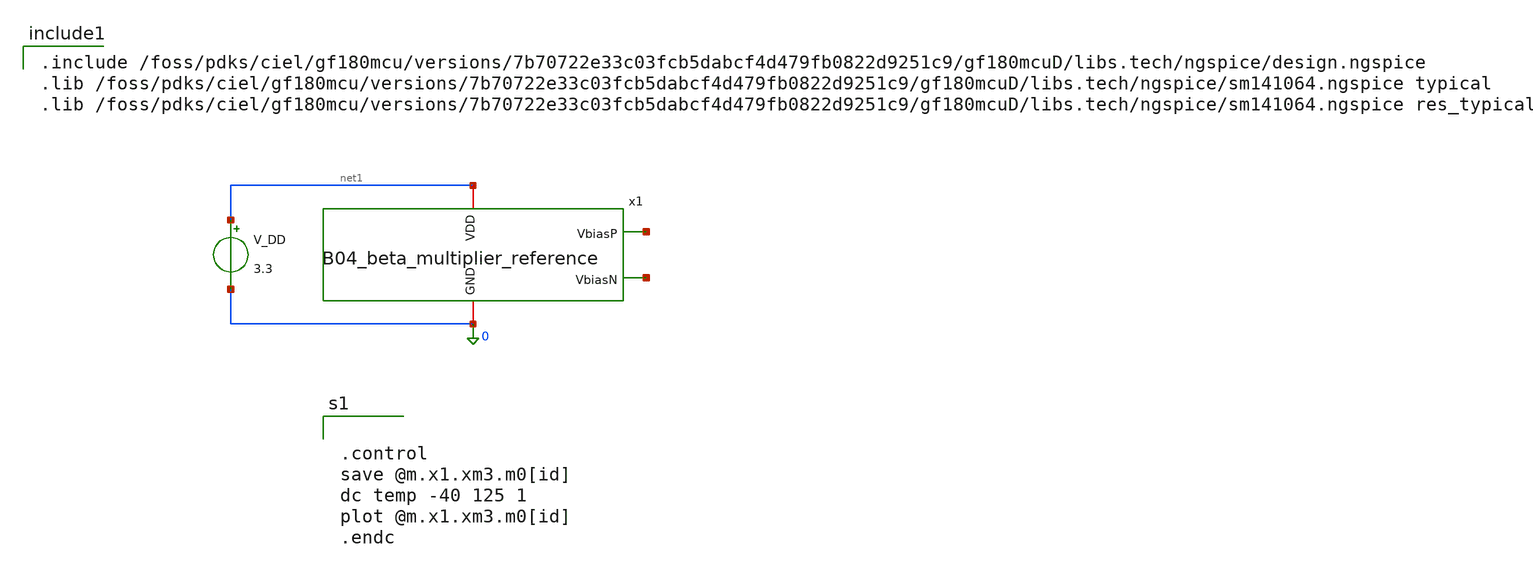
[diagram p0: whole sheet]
** sch_path: analog/B04_tb_beta_multiplier_reference.sch
**.subckt B04_tb_beta_multiplier_reference
x1 net1 net2 net3 0 B04_beta_multiplier_reference length=410u
V_DD net1 0 3.3
**** begin user architecture code


.control
save @m.x1.xm3.m0[id]
dc temp -40 125 1
plot @m.x1.xm3.m0[id]
.endc



.include /foss/pdks/ciel/gf180mcu/versions/7b70722e33c03fcb5dabcf4d479fb0822d9251c9/gf180mcuD/libs.tech/ngspice/design.ngspice
.lib /foss/pdks/ciel/gf180mcu/versions/7b70722e33c03fcb5dabcf4d479fb0822d9251c9/gf180mcuD/libs.tech/ngspice/sm141064.ngspice typical
.lib /foss/pdks/ciel/gf180mcu/versions/7b70722e33c03fcb5dabcf4d479fb0822d9251c9/gf180mcuD/libs.tech/ngspice/sm141064.ngspice res_typical

**** end user architecture code
**.ends

* expanding   symbol:
*+  AURA-Event-Driven-Mixed-Signal-ASIC-for-Acoustic-Pattern-Detection/analog/B04_beta_multiplier_reference.sym # of pins=4
** sym_path: analog/B04_beta_multiplier_reference.sym
** sch_path: analog/B04_beta_multiplier_reference.sch
.subckt B04_beta_multiplier_reference VDD VbiasP VbiasN GND  length=410u
*.iopin VDD
*.iopin GND
*.opin VbiasP
*.opin VbiasN
XM2 VbiasN VbiasP VDD VDD pfet_03v3 L=4u W=2u nf=1 ad='int((nf+1)/2) * W/nf * 0.18u' as='int((nf+2)/2) * W/nf * 0.18u'
+ pd='2*int((nf+1)/2) * (W/nf + 0.18u)' ps='2*int((nf+2)/2) * (W/nf + 0.18u)' nrd='0.18u / W' nrs='0.18u / W'
+ sa=0 sb=0 sd=0 m=1
XM3 net2 VbiasP VDD VDD pfet_03v3 L=4u W=2u nf=1 ad='int((nf+1)/2) * W/nf * 0.18u' as='int((nf+2)/2) * W/nf * 0.18u'
+ pd='2*int((nf+1)/2) * (W/nf + 0.18u)' ps='2*int((nf+2)/2) * (W/nf + 0.18u)' nrd='0.18u / W' nrs='0.18u / W'
+ sa=0 sb=0 sd=0 m=1
XM6 VbiasN VbiasN GND GND nfet_03v3 L=4u W=10u nf=1 ad='int((nf+1)/2) * W/nf * 0.18u' as='int((nf+2)/2) * W/nf * 0.18u'
+ pd='2*int((nf+1)/2) * (W/nf + 0.18u)' ps='2*int((nf+2)/2) * (W/nf + 0.18u)' nrd='0.18u / W' nrs='0.18u / W'
+ sa=0 sb=0 sd=0 m=1
XM7 net2 VbiasN net1 GND nfet_03v3 L=4u W=10u nf=1 ad='int((nf+1)/2) * W/nf * 0.18u' as='int((nf+2)/2) * W/nf * 0.18u'
+ pd='2*int((nf+1)/2) * (W/nf + 0.18u)' ps='2*int((nf+2)/2) * (W/nf + 0.18u)' nrd='0.18u / W' nrs='0.18u / W'
+ sa=0 sb=0 sd=0 m=4
XM1 net4 net4 VDD VDD pfet_03v3 L=40u W=0.22u nf=1 ad='int((nf+1)/2) * W/nf * 0.18u' as='int((nf+2)/2) * W/nf * 0.18u'
+ pd='2*int((nf+1)/2) * (W/nf + 0.18u)' ps='2*int((nf+2)/2) * (W/nf + 0.18u)' nrd='0.18u / W' nrs='0.18u / W'
+ sa=0 sb=0 sd=0 m=1
XM4 VbiasP net3 VbiasN GND nfet_03v3 L=1u W=1u nf=1 ad='int((nf+1)/2) * W/nf * 0.18u' as='int((nf+2)/2) * W/nf * 0.18u'
+ pd='2*int((nf+1)/2) * (W/nf + 0.18u)' ps='2*int((nf+2)/2) * (W/nf + 0.18u)' nrd='0.18u / W' nrs='0.18u / W'
+ sa=0 sb=0 sd=0 m=1
XM5 net3 VbiasN GND GND nfet_03v3 L=10u W=1u nf=1 ad='int((nf+1)/2) * W/nf * 0.18u' as='int((nf+2)/2) * W/nf * 0.18u'
+ pd='2*int((nf+1)/2) * (W/nf + 0.18u)' ps='2*int((nf+2)/2) * (W/nf + 0.18u)' nrd='0.18u / W' nrs='0.18u / W'
+ sa=0 sb=0 sd=0 m=1
XM8 net5 net5 net4 VDD pfet_03v3 L=40u W=0.22u nf=1 ad='int((nf+1)/2) * W/nf * 0.18u' as='int((nf+2)/2) * W/nf * 0.18u'
+ pd='2*int((nf+1)/2) * (W/nf + 0.18u)' ps='2*int((nf+2)/2) * (W/nf + 0.18u)' nrd='0.18u / W' nrs='0.18u / W'
+ sa=0 sb=0 sd=0 m=1
XM9 net3 net5 net5 VDD pfet_03v3 L=40u W=0.22u nf=1 ad='int((nf+1)/2) * W/nf * 0.18u' as='int((nf+2)/2) * W/nf * 0.18u'
+ pd='2*int((nf+1)/2) * (W/nf + 0.18u)' ps='2*int((nf+2)/2) * (W/nf + 0.18u)' nrd='0.18u / W' nrs='0.18u / W'
+ sa=0 sb=0 sd=0 m=1
XR2 GND net1 GND ppolyf_u_2k r_width=2u r_length={length} m=1
x1 VDD VbiasP net2 VbiasN VbiasN GND B04_diff_amp
.ends


* expanding   symbol:
*+  AURA-Event-Driven-Mixed-Signal-ASIC-for-Acoustic-Pattern-Detection/analog/B04_diff_amp.sym # of pins=6
** sym_path: analog/B04_diff_amp.sym
** sch_path: analog/B04_diff_amp.sch
.subckt B04_diff_amp VDD Vo V+ V- Vbias VSS
*.iopin VDD
*.iopin VSS
*.ipin V+
*.ipin V-
*.opin Vo
*.ipin Vbias
XM1 net1 V+ net2 VSS nfet_03v3 L=4u W=1.1u nf=1 ad='int((nf+1)/2) * W/nf * 0.18u' as='int((nf+2)/2) * W/nf * 0.18u'
+ pd='2*int((nf+1)/2) * (W/nf + 0.18u)' ps='2*int((nf+2)/2) * (W/nf + 0.18u)' nrd='0.18u / W' nrs='0.18u / W'
+ sa=0 sb=0 sd=0 m=1
XM2 net2 Vbias VSS VSS nfet_03v3 L=4u W=2.2u nf=1 ad='int((nf+1)/2) * W/nf * 0.18u' as='int((nf+2)/2) * W/nf * 0.18u'
+ pd='2*int((nf+1)/2) * (W/nf + 0.18u)' ps='2*int((nf+2)/2) * (W/nf + 0.18u)' nrd='0.18u / W' nrs='0.18u / W'
+ sa=0 sb=0 sd=0 m=1
XM3 Vo V- net2 VSS nfet_03v3 L=4u W=1.1u nf=1 ad='int((nf+1)/2) * W/nf * 0.18u' as='int((nf+2)/2) * W/nf * 0.18u'
+ pd='2*int((nf+1)/2) * (W/nf + 0.18u)' ps='2*int((nf+2)/2) * (W/nf + 0.18u)' nrd='0.18u / W' nrs='0.18u / W'
+ sa=0 sb=0 sd=0 m=1
XM4 Vo net1 VDD VDD pfet_03v3 L=4u W=13u nf=1 ad='int((nf+1)/2) * W/nf * 0.18u' as='int((nf+2)/2) * W/nf * 0.18u'
+ pd='2*int((nf+1)/2) * (W/nf + 0.18u)' ps='2*int((nf+2)/2) * (W/nf + 0.18u)' nrd='0.18u / W' nrs='0.18u / W'
+ sa=0 sb=0 sd=0 m=1
XM5 net1 net1 VDD VDD pfet_03v3 L=4u W=13u nf=1 ad='int((nf+1)/2) * W/nf * 0.18u' as='int((nf+2)/2) * W/nf * 0.18u'
+ pd='2*int((nf+1)/2) * (W/nf + 0.18u)' ps='2*int((nf+2)/2) * (W/nf + 0.18u)' nrd='0.18u / W' nrs='0.18u / W'
+ sa=0 sb=0 sd=0 m=1
XMDummy VDD VDD VDD VDD pfet_03v3 L=4u W=6.5u nf=1 ad='int((nf+1)/2) * W/nf * 0.18u' as='int((nf+2)/2) * W/nf * 0.18u'
+ pd='2*int((nf+1)/2) * (W/nf + 0.18u)' ps='2*int((nf+2)/2) * (W/nf + 0.18u)' nrd='0.18u / W' nrs='0.18u / W'
+ sa=0 sb=0 sd=0 m=1
XMDummy1 VDD VDD VDD VDD pfet_03v3 L=4u W=6.5u nf=1 ad='int((nf+1)/2) * W/nf * 0.18u' as='int((nf+2)/2) * W/nf * 0.18u'
+ pd='2*int((nf+1)/2) * (W/nf + 0.18u)' ps='2*int((nf+2)/2) * (W/nf + 0.18u)' nrd='0.18u / W' nrs='0.18u / W'
+ sa=0 sb=0 sd=0 m=1
XMdummy2 VSS VSS VSS VSS nfet_03v3 L=4u W=0.55u nf=1 ad='int((nf+1)/2) * W/nf * 0.18u' as='int((nf+2)/2) * W/nf * 0.18u'
+ pd='2*int((nf+1)/2) * (W/nf + 0.18u)' ps='2*int((nf+2)/2) * (W/nf + 0.18u)' nrd='0.18u / W' nrs='0.18u / W'
+ sa=0 sb=0 sd=0 m=1
XMdummy3 VSS VSS VSS VSS nfet_03v3 L=4u W=0.55u nf=1 ad='int((nf+1)/2) * W/nf * 0.18u' as='int((nf+2)/2) * W/nf * 0.18u'
+ pd='2*int((nf+1)/2) * (W/nf + 0.18u)' ps='2*int((nf+2)/2) * (W/nf + 0.18u)' nrd='0.18u / W' nrs='0.18u / W'
+ sa=0 sb=0 sd=0 m=1
.ends

.end
